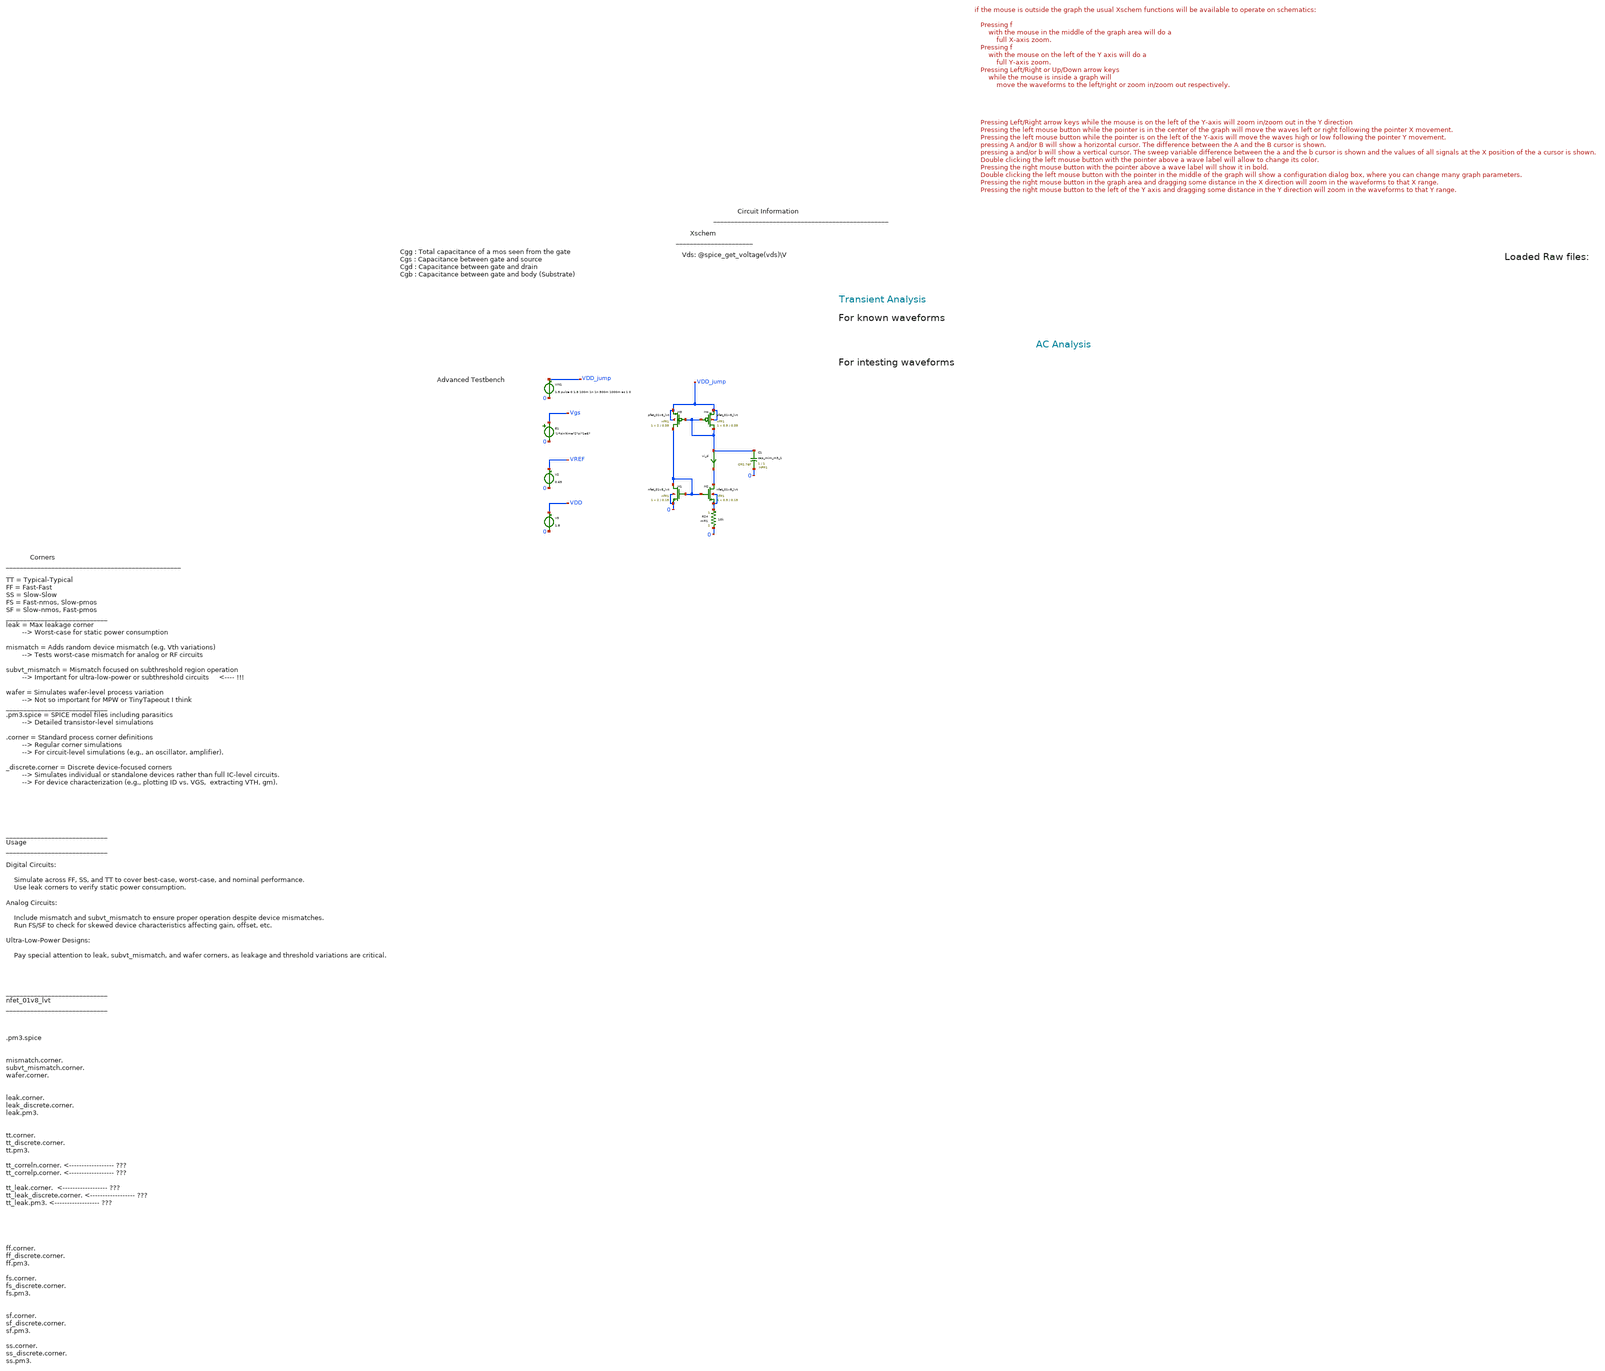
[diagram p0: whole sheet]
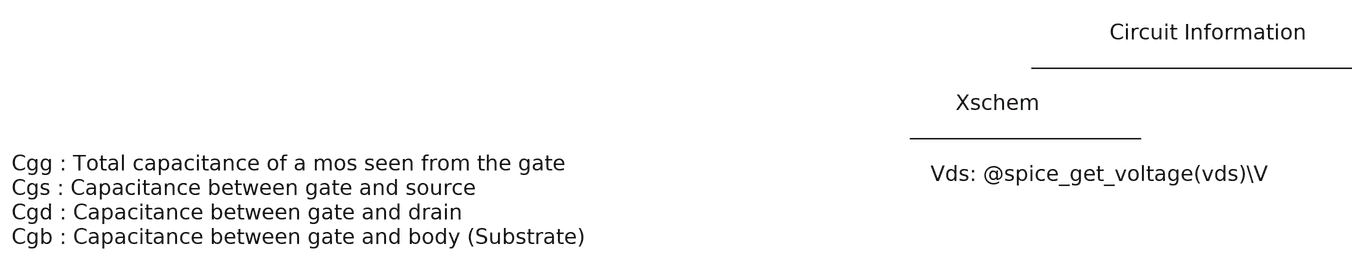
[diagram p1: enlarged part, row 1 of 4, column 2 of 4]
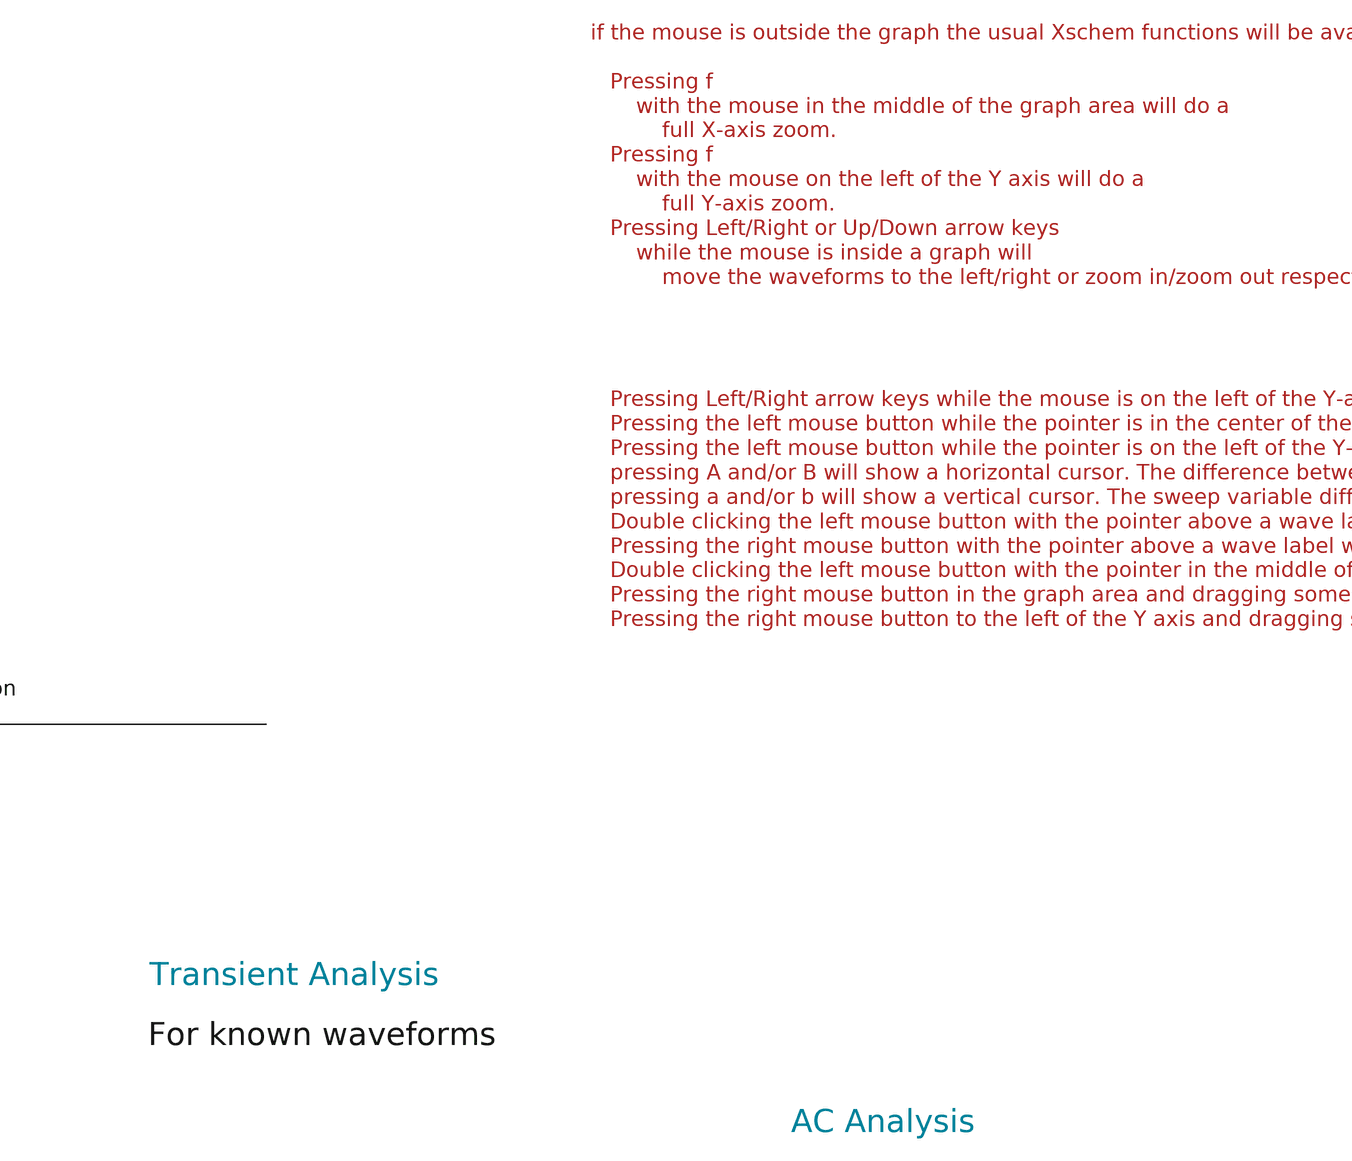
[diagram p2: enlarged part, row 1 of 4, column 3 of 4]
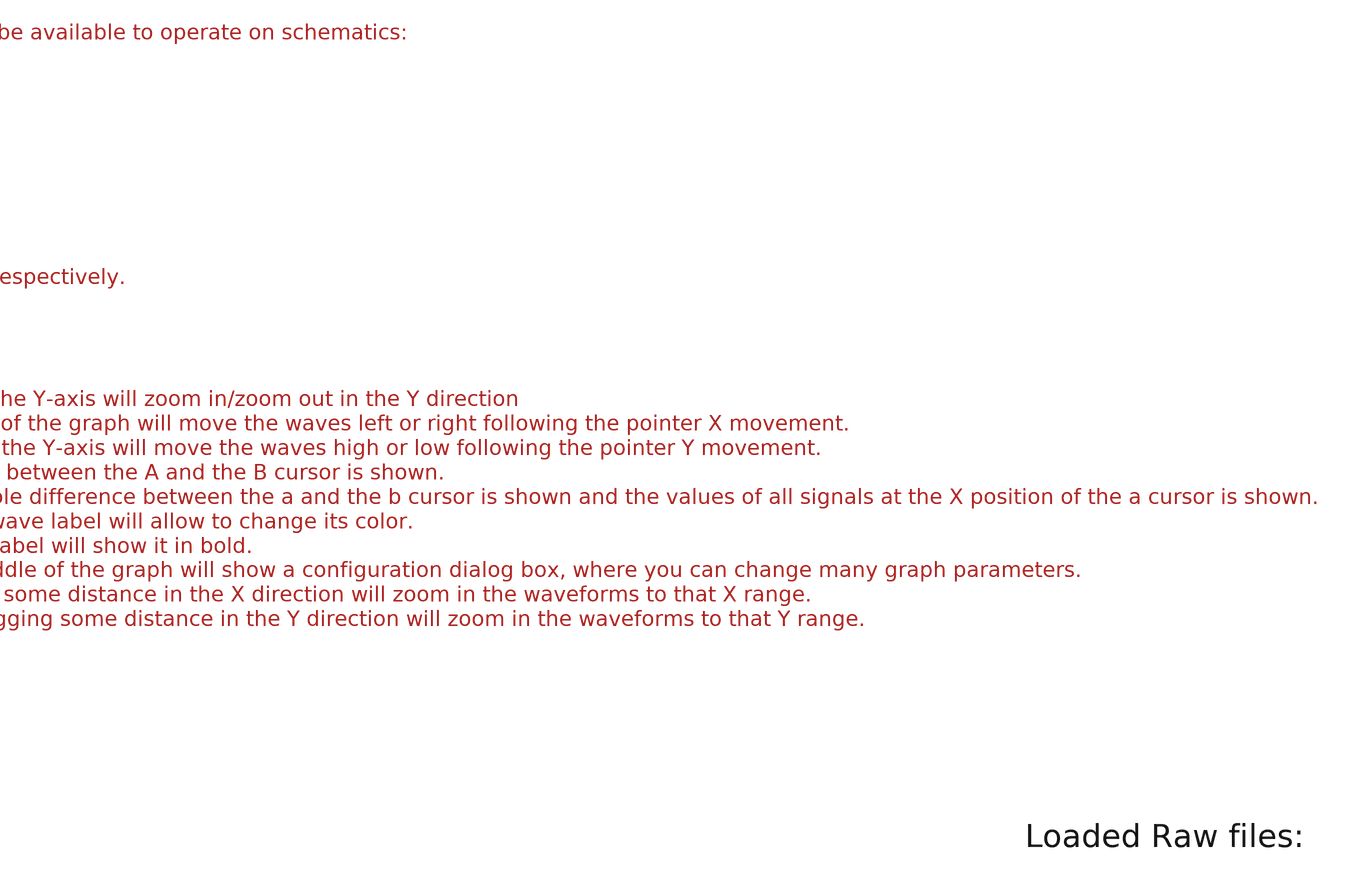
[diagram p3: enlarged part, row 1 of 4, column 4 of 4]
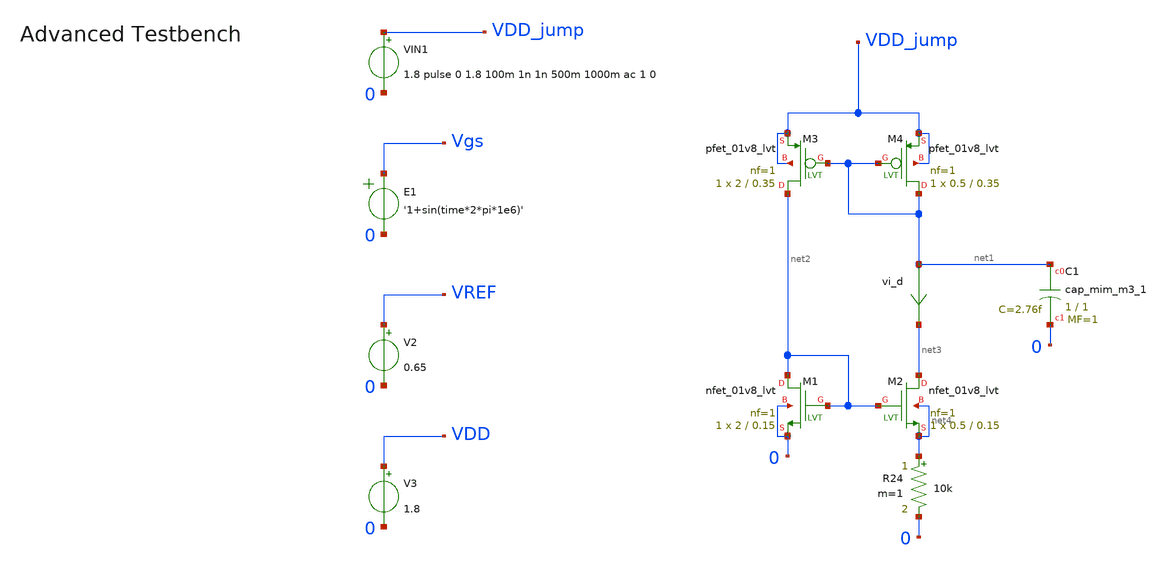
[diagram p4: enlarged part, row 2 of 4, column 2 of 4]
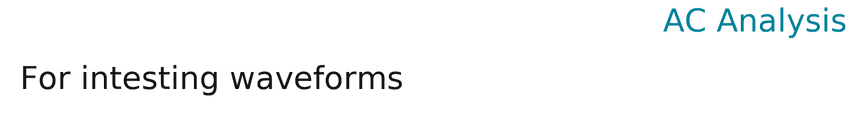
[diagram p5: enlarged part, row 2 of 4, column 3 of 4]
** sch_path: tt10-hdl/tt_um_test_commit/xschem/T0/currMirr/curr_mirror_basic_tb.sch
* Copyright (C) 1998-2024 Stefan Frederik Schippers
* This program is free software; you can redistribute it and/or modify
* it under the terms of the GNU General Public License as published by
* the Free Software Foundation; either version 2 of the License, or
* (at your option) any later version.
* This program is distributed in the hope that it will be useful,
* but WITHOUT ANY WARRANTY; without even the implied warranty of
* MERCHANTABILITY or FITNESS FOR A PARTICULAR PURPOSE.  See the
* GNU General Public License for more details.
* You should have received a copy of the GNU General Public License
* along with this program; if not, write to the Free Software
**.subckt curr_mirror_basic_tb
vi_d net1 net3 0
.save i(vi_d)
V2 VREF 0 0.65
E1 Vgs 0 VOL=' '1+sin(time*2*pi*1e6)' '
XM1 net2 net2 0 0 sky130_fd_pr__nfet_01v8_lvt L=0.15 W=2 nf=1 ad='int((1 + 1)/2) * 2 / 1 * 0.29' as='int((1 + 2)/2) * 2 / 1 * 0.29'
+ pd='2*int((1 + 1)/2) * (2 / 1 + 0.29)' ps='2*int((1 + 2)/2) * (2 / 1 + 0.29)' nrd='0.29 / 2 ' nrs='0.29 / 2 '
+ sa=0 sb=0 sd=0 mult=1 m=1
V3 VDD 0 1.8
XM2 net3 net2 net4 net4 sky130_fd_pr__nfet_01v8_lvt L=0.15 W=0.5 nf=1 ad='int((1 + 1)/2) * 0.5 / 1 * 0.29'
+ as='int((1 + 2)/2) * 0.5 / 1 * 0.29' pd='2*int((1 + 1)/2) * (0.5 / 1 + 0.29)' ps='2*int((1 + 2)/2) * (0.5 / 1 + 0.29)'
+ nrd='0.29 / 0.5 ' nrs='0.29 / 0.5 ' sa=0 sb=0 sd=0 mult=1 m=1
R24 net4 0 10k m=1
XM3 net2 net1 VDD_jump VDD_jump sky130_fd_pr__pfet_01v8_lvt L=0.35 W=2 nf=1 ad='int((1 + 1)/2) * 2 / 1 * 0.29'
+ as='int((1 + 2)/2) * 2 / 1 * 0.29' pd='2*int((1 + 1)/2) * (2 / 1 + 0.29)' ps='2*int((1 + 2)/2) * (2 / 1 + 0.29)'
+ nrd='0.29 / 2 ' nrs='0.29 / 2 ' sa=0 sb=0 sd=0 mult=1 m=1
XM4 net1 net1 VDD_jump VDD_jump sky130_fd_pr__pfet_01v8_lvt L=0.35 W=0.5 nf=1 ad='int((1 + 1)/2) * 0.5 / 1 * 0.29'
+ as='int((1 + 2)/2) * 0.5 / 1 * 0.29' pd='2*int((1 + 1)/2) * (0.5 / 1 + 0.29)' ps='2*int((1 + 2)/2) * (0.5 / 1 + 0.29)'
+ nrd='0.29 / 0.5 ' nrs='0.29 / 0.5 ' sa=0 sb=0 sd=0 mult=1 m=1
XC1 net1 0 sky130_fd_pr__cap_mim_m3_1 W=1 L=1 MF=1 m=1
VIN1 VDD_jump 0 1.8 pulse 0 1.8 100m 1n 1n 500m 1000m ac 1 0
**** begin user architecture code



.temp 30

*.option gmin=5n
*.option scale=1e-6
.option wnflag=1
.option savecurrents

.save all
.control
  save all alli

  save @m.xm1.msky130_fd_pr__nfet_01v8_lvt[gm]
  save @m.xm1.msky130_fd_pr__nfet_01v8_lvt[id]
  save @m.xm1.msky130_fd_pr__nfet_01v8_lvt[vgs]

  save @m.xm1.msky130_fd_pr__nfet_01v8_lvt[cgg]
  save @m.xm1.msky130_fd_pr__nfet_01v8_lvt[cgs]
  save @m.xm1.msky130_fd_pr__nfet_01v8_lvt[cgdo]
  save @m.xm1.msky130_fd_pr__nfet_01v8_lvt[cgb]

  save @m.xm1.msky130_fd_pr__nfet_01v8_lvt[vds]
  save @m.xm1.msky130_fd_pr__nfet_01v8_lvt[vdsat]
  save @m.xm1.msky130_fd_pr__nfet_01v8_lvt[vth]


  save @m.xm1.msky130_fd_pr__nfet_01v8_lvt[leff]
  save @m.xm1.msky130_fd_pr__nfet_01v8_lvt[weff]
  save @m.xm1.msky130_fd_pr__nfet_01v8_lvt[gds]
  save @m.xm1.msky130_fd_pr__nfet_01v8_lvt[l]
  save @m.xm1.msky130_fd_pr__nfet_01v8_lvt[w]
  save @m.xm1.msky130_fd_pr__nfet_01v8_lvt[gm]
  save @m.xm1.msky130_fd_pr__nfet_01v8_lvt[gm]
  save @m.xm1.msky130_fd_pr__nfet_01v8_lvt[gm]
  save @m.xm1.msky130_fd_pr__nfet_01v8_lvt[gm]
  save @m.xm1.msky130_fd_pr__nfet_01v8_lvt[gm]



  *dc v_dev_vds 0 1.8 0.005 v_dev_vgs 0 1.8 0.2
  *write nmos_tb.raw




  tran 1m 5000m
  write nmos_tb_tran.raw

  op
  set appendwrite
  write nmos_tb_tran.raw






  *quit 0




.endc





** opencircuitdesign pdks install
.lib $::SKYWATER_MODELS/sky130.lib.spice tt
.include $::SKYWATER_STDCELLS/sky130_fd_sc_hd.spice


**** end user architecture code
**.ends
.end
